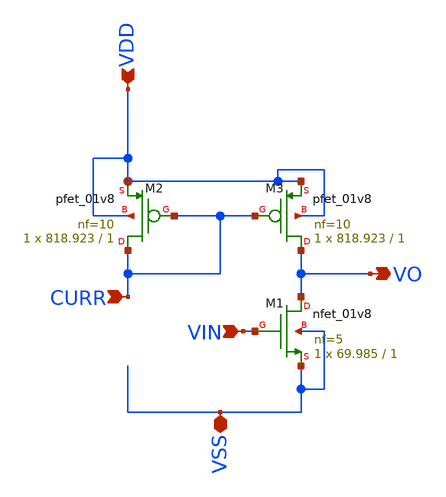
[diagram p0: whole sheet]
** sch_path: cs.sch
**.subckt cs VDD VIN VO VSS CURR
*.ipin VDD
*.ipin VIN
*.opin VO
*.iopin VSS
*.ipin CURR
XM1 VO VIN VSS VSS sky130_fd_pr__nfet_01v8 L=1 W=69.985 nf=5 ad='int((5 + 1)/2) * 69.985 / 5 * 0.29'
+ as='int((5 + 2)/2) * 69.985 / 5 * 0.29' pd='2*int((5 + 1)/2) * (69.985 / 5 + 0.29)' ps='2*int((5 + 2)/2) * (69.985 / 5 + 0.29)'
+ nrd='0.29 / 69.985 ' nrs='0.29 / 69.985 ' sa=0 sb=0 sd=0 mult=1 m=1
XM2 CURR CURR VDD VDD sky130_fd_pr__pfet_01v8 L=1 W=818.923 nf=10 ad='int((10 + 1)/2) * 818.923 / 10 * 0.29'
+ as='int((10 + 2)/2) * 818.923 / 10 * 0.29' pd='2*int((10 + 1)/2) * (818.923 / 10 + 0.29)' ps='2*int((10 + 2)/2) * (818.923 / 10 + 0.29)'
+ nrd='0.29 / 818.923 ' nrs='0.29 / 818.923 ' sa=0 sb=0 sd=0 mult=1 m=1
XM3 VO CURR VDD VDD sky130_fd_pr__pfet_01v8 L=1 W=818.923 nf=10 ad='int((10 + 1)/2) * 818.923 / 10 * 0.29'
+ as='int((10 + 2)/2) * 818.923 / 10 * 0.29' pd='2*int((10 + 1)/2) * (818.923 / 10 + 0.29)' ps='2*int((10 + 2)/2) * (818.923 / 10 + 0.29)'
+ nrd='0.29 / 818.923 ' nrs='0.29 / 818.923 ' sa=0 sb=0 sd=0 mult=1 m=1
**.ends
.end
